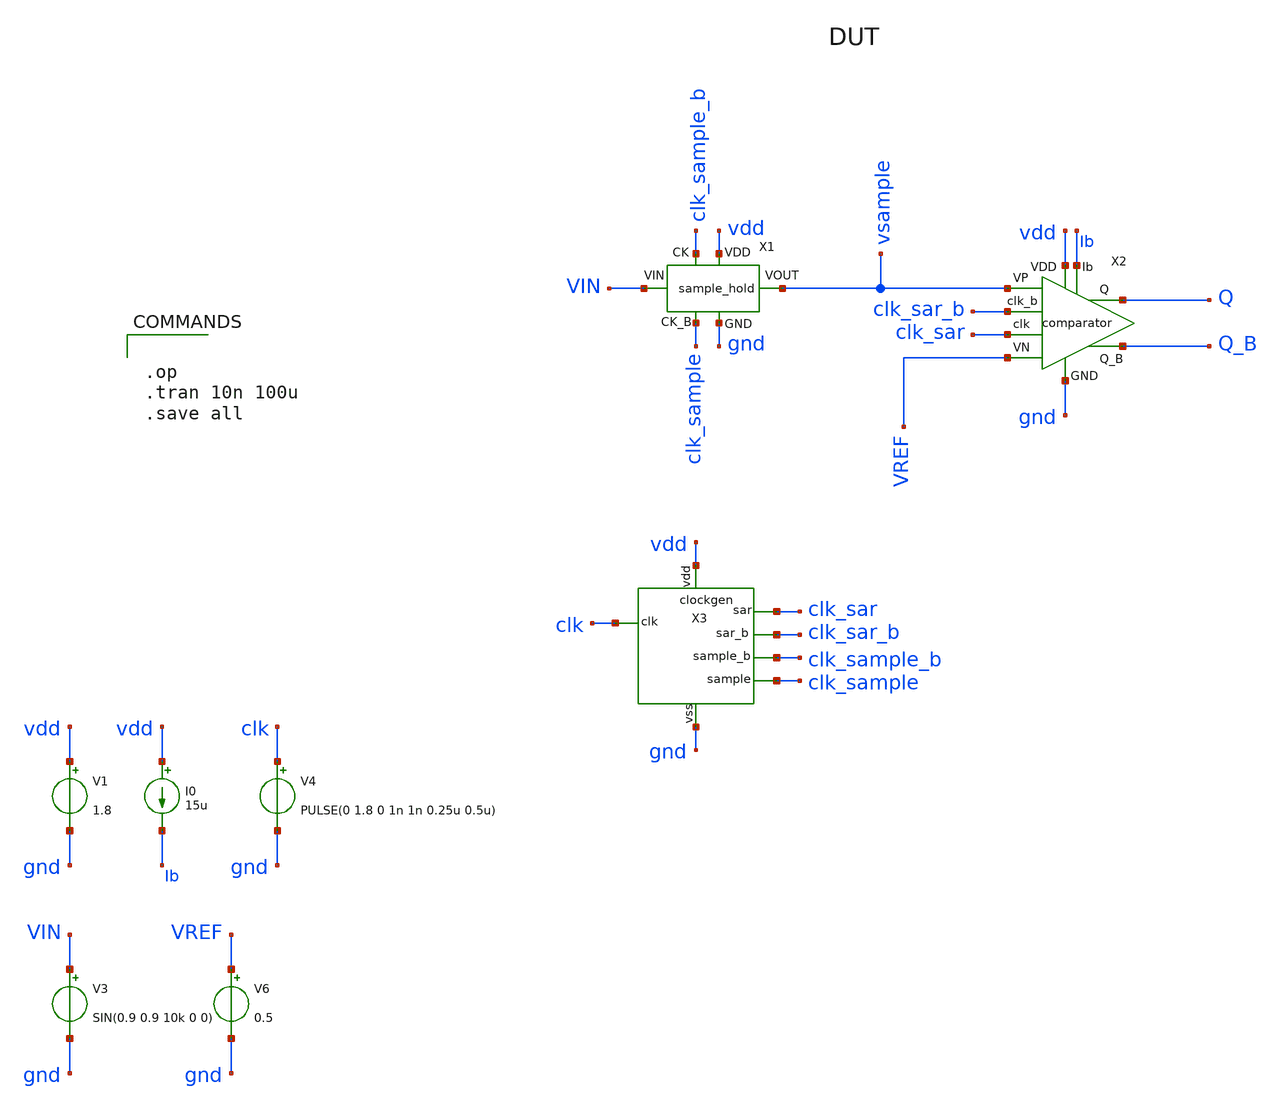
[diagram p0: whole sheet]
** sch_path: xschem/adc_top.sch
.lib $::SKYWATER_MODELS/sky130.lib.spice tt
.include $::SKYWATER_STDCELLS/sky130_fd_sc_hd.spice

**.subckt adc_top
V1 vdd gnd 1.8
V3 VIN gnd SIN(0.9 0.9 10k 0 0)
V4 clk gnd PULSE(0 1.8 0 1n 1n 0.25u 0.5u)
V6 VREF gnd 0.5
I0 vdd Ib 15u
X2 vsample VREF gnd Q_B Q vdd clk_sar Ib clk_sar_b comparator
X1 gnd vdd VIN vsample clk_sample_b clk_sample sample_hold
X3 clk vdd clk_sar clk_sample gnd clk_sar_b clk_sample_b clockgen
**** begin user architecture code


.op
.tran 10n 100u
.save all


**** end user architecture code
**.ends
.end
